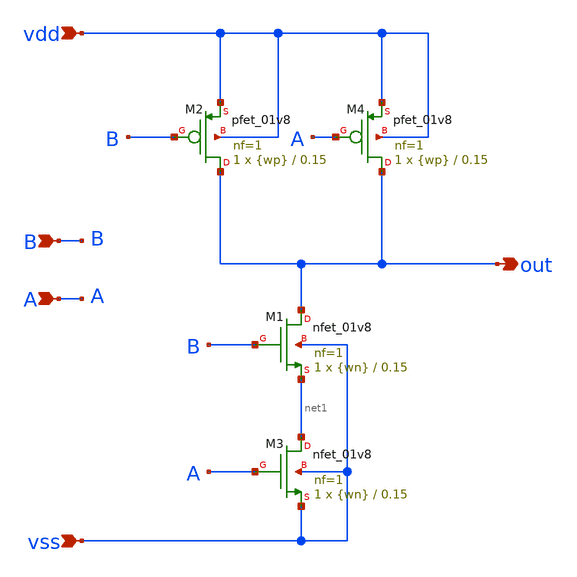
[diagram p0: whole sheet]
** sch_path: src/nand/nand.sch
**.subckt nand B A vss vdd out
*.ipin B
*.ipin A
*.ipin vss
*.ipin vdd
*.opin out
XM1 out B net1 vss sky130_fd_pr__nfet_01v8 L=0.15 W={wn} nf=1 ad='int((nf+1)/2) * W/nf * 0.29' as='int((nf+2)/2) * W/nf * 0.29'
+ pd='2*int((nf+1)/2) * (W/nf + 0.29)' ps='2*int((nf+2)/2) * (W/nf + 0.29)' nrd='0.29 / W' nrs='0.29 / W'
+ sa=0 sb=0 sd=0 mult=1 m=1
XM2 out B vdd vdd sky130_fd_pr__pfet_01v8 L=0.15 W={wp} nf=1 ad='int((nf+1)/2) * W/nf * 0.29' as='int((nf+2)/2) * W/nf * 0.29'
+ pd='2*int((nf+1)/2) * (W/nf + 0.29)' ps='2*int((nf+2)/2) * (W/nf + 0.29)' nrd='0.29 / W' nrs='0.29 / W'
+ sa=0 sb=0 sd=0 mult=1 m=1
XM3 net1 A vss vss sky130_fd_pr__nfet_01v8 L=0.15 W={wn} nf=1 ad='int((nf+1)/2) * W/nf * 0.29' as='int((nf+2)/2) * W/nf * 0.29'
+ pd='2*int((nf+1)/2) * (W/nf + 0.29)' ps='2*int((nf+2)/2) * (W/nf + 0.29)' nrd='0.29 / W' nrs='0.29 / W'
+ sa=0 sb=0 sd=0 mult=1 m=1
XM4 out A vdd vdd sky130_fd_pr__pfet_01v8 L=0.15 W={wp} nf=1 ad='int((nf+1)/2) * W/nf * 0.29' as='int((nf+2)/2) * W/nf * 0.29'
+ pd='2*int((nf+1)/2) * (W/nf + 0.29)' ps='2*int((nf+2)/2) * (W/nf + 0.29)' nrd='0.29 / W' nrs='0.29 / W'
+ sa=0 sb=0 sd=0 mult=1 m=1
**.ends
.end
